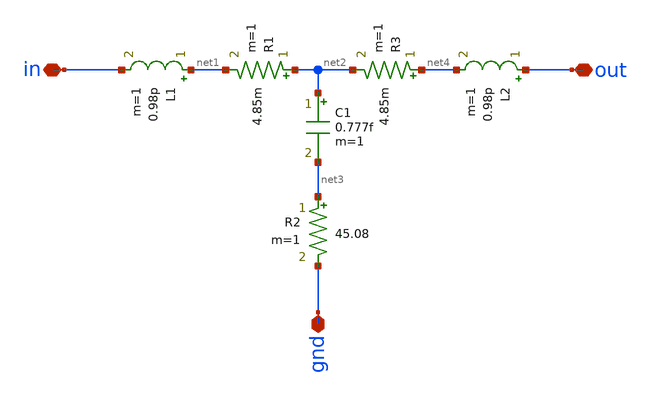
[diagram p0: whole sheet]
** sch_path: VGA_tapeout/xschem/sims/SCPWm1_segment_3p65um.sch
**.subckt SCPWm1_segment_3p65um in out gnd
*.iopin in
*.iopin out
*.iopin gnd
L1 net1 in 0.98p m=1
C1 net2 net3 0.777f m=1
R1 net2 net1 4.85m m=1
R2 net3 gnd 45.08 m=1
R3 net4 net2 4.85m m=1
L2 out net4 0.98p m=1
**.ends
.end
